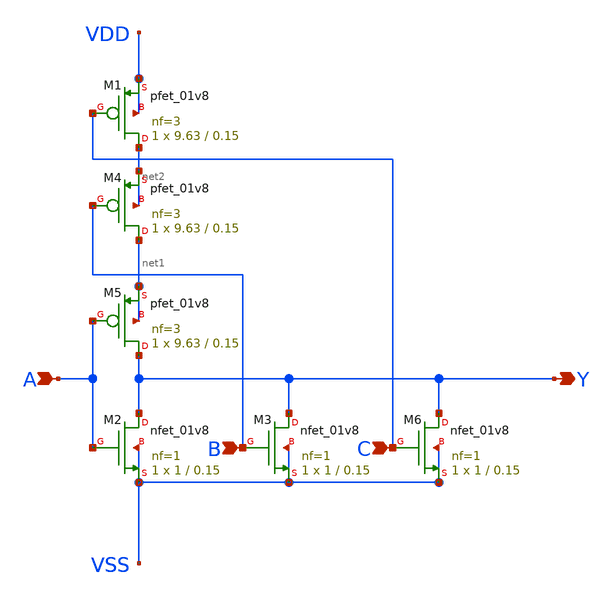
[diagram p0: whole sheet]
** sch_path: design/xschem/NOR/nor3.sch
**.subckt nor3 A Y B B C
*.ipin A
*.opin Y
*.ipin B
*.ipin B
*.ipin C
XM2 Y A VSS VSS sky130_fd_pr__nfet_01v8 L=0.15 W=1 nf=1 ad='int((nf+1)/2) * W/nf * 0.29' as='int((nf+2)/2) * W/nf * 0.29'
+ pd='2*int((nf+1)/2) * (W/nf + 0.29)' ps='2*int((nf+2)/2) * (W/nf + 0.29)' nrd='0.29 / W' nrs='0.29 / W'
+ sa=0 sb=0 sd=0 mult=1 m=1
XM3 Y B VSS VSS sky130_fd_pr__nfet_01v8 L=0.15 W=1 nf=1 ad='int((nf+1)/2) * W/nf * 0.29' as='int((nf+2)/2) * W/nf * 0.29'
+ pd='2*int((nf+1)/2) * (W/nf + 0.29)' ps='2*int((nf+2)/2) * (W/nf + 0.29)' nrd='0.29 / W' nrs='0.29 / W'
+ sa=0 sb=0 sd=0 mult=1 m=1
XM6 Y C VSS VSS sky130_fd_pr__nfet_01v8 L=0.15 W=1 nf=1 ad='int((nf+1)/2) * W/nf * 0.29' as='int((nf+2)/2) * W/nf * 0.29'
+ pd='2*int((nf+1)/2) * (W/nf + 0.29)' ps='2*int((nf+2)/2) * (W/nf + 0.29)' nrd='0.29 / W' nrs='0.29 / W'
+ sa=0 sb=0 sd=0 mult=1 m=1
XM1 net2 C VDD VDD sky130_fd_pr__pfet_01v8 L=0.15 W=9.63 nf=3 ad='int((nf+1)/2) * W/nf * 0.29' as='int((nf+2)/2) * W/nf * 0.29'
+ pd='2*int((nf+1)/2) * (W/nf + 0.29)' ps='2*int((nf+2)/2) * (W/nf + 0.29)' nrd='0.29 / W' nrs='0.29 / W'
+ sa=0 sb=0 sd=0 mult=1 m=1
XM4 net1 B net2 net2 sky130_fd_pr__pfet_01v8 L=0.15 W=9.63 nf=3 ad='int((nf+1)/2) * W/nf * 0.29' as='int((nf+2)/2) * W/nf * 0.29'
+ pd='2*int((nf+1)/2) * (W/nf + 0.29)' ps='2*int((nf+2)/2) * (W/nf + 0.29)' nrd='0.29 / W' nrs='0.29 / W'
+ sa=0 sb=0 sd=0 mult=1 m=1
XM5 Y A net1 net1 sky130_fd_pr__pfet_01v8 L=0.15 W=9.63 nf=3 ad='int((nf+1)/2) * W/nf * 0.29' as='int((nf+2)/2) * W/nf * 0.29'
+ pd='2*int((nf+1)/2) * (W/nf + 0.29)' ps='2*int((nf+2)/2) * (W/nf + 0.29)' nrd='0.29 / W' nrs='0.29 / W'
+ sa=0 sb=0 sd=0 mult=1 m=1
**.ends
.end
